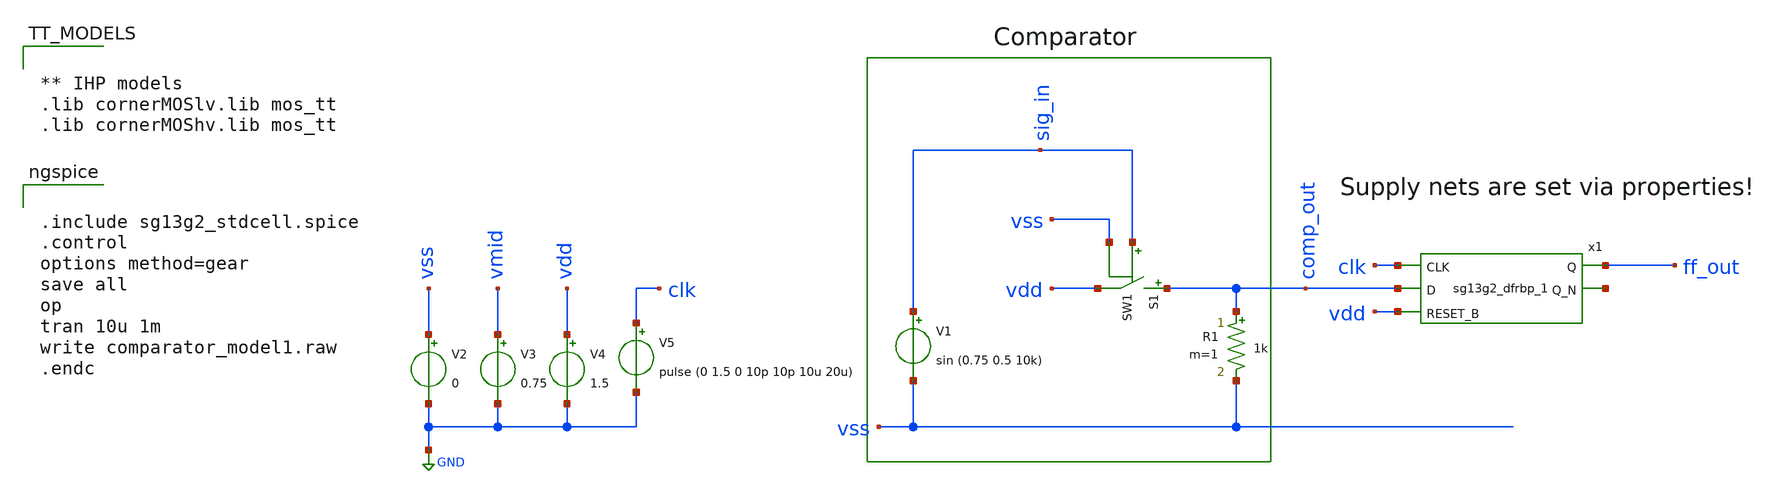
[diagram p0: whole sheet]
** sch_path: 10_xschem/comparator_model1.sch
**.subckt comparator_model1
S1 comp_out vdd sig_in vss SW1
R1 comp_out vss 1k m=1
V1 sig_in vss sin (0.75 0.5 10k)
V2 vss GND 0
V3 vmid GND 0.75
V4 vdd GND 1.5
x1 ff_out net1 clk comp_out vdd vdd vss sg13g2_dfrbp_1
V5 clk GND pulse (0 1.5 0 10p 10p 10u 20u)
**** begin user architecture code


.include sg13g2_stdcell.spice
.control
options method=gear
save all
op
tran 10u 1m
write comparator_model1.raw
.endc




** IHP models
.lib cornerMOSlv.lib mos_tt
.lib cornerMOShv.lib mos_tt


**** end user architecture code
**.ends

* expanding   symbol:  sg13g2_stdcells/sg13g2_dfrbp_1.sym # of pins=5
** sym_path: sg13g2_stdcells/sg13g2_dfrbp_1.sym
** sch_path: sg13g2_stdcells/sg13g2_dfrbp_1.sch
.subckt sg13g2_dfrbp_1 Q Q_N CLK D RESET_B VDD VSS
*.ipin D
*.ipin RESET_B
*.ipin CLK
*.opin Q
*.opin Q_N
*.iopin VDD
*.iopin VSS
XM1 Db D net10 VSS sg13_lv_nmos w=420.00n l=130.00n ng=1 m=1 mm_ok=1
XM2 net10 RESET_B VSS VSS sg13_lv_nmos w=420.00n l=130.00n ng=1 m=1 mm_ok=1
XM3 net1 clkneg net9 VSS sg13_lv_nmos w=420.00n l=130.00n ng=1 m=1 mm_ok=1
XM4 net9 net1 VSS VSS sg13_lv_nmos w=420.00n l=130.00n ng=1 m=1 mm_ok=1
XM5 net1 net1 net5 VSS sg13_lv_nmos w=420.00n l=130.00n ng=1 m=1 mm_ok=1
XM6 net5 RESET_B VSS VSS sg13_lv_nmos w=420.00n l=130.00n ng=1 m=1 mm_ok=1
XM7 Q_N net1 VSS VSS sg13_lv_nmos w=740.00n l=130.00n ng=1 m=1 mm_ok=1
XM8 net2 net1 VSS VSS sg13_lv_nmos w=740.00n l=130.00n ng=1 m=1 mm_ok=1
XM9 Q net2 VSS VSS sg13_lv_nmos w=740.00n l=130.00n ng=1 m=1 mm_ok=1
XM10 clkneg CLK VSS VSS sg13_lv_nmos w=740.00n l=130.00n ng=1 m=1 mm_ok=1
XM11 clkpos clkneg VSS VSS sg13_lv_nmos w=740.00n l=130.00n ng=1 m=1 mm_ok=1
XM12 Db clkneg net3 VSS sg13_lv_nmos w=420.00n l=130.00n ng=1 m=1 mm_ok=1
XM13 net3 clkpos net8 VSS sg13_lv_nmos w=420.00n l=130.00n ng=1 m=1 mm_ok=1
XM14 net8 net3 net4 VSS sg13_lv_nmos w=420.00n l=130.00n ng=1 m=1 mm_ok=1
XM15 net4 RESET_B VSS VSS sg13_lv_nmos w=420.00n l=130.00n ng=1 m=1 mm_ok=1
XM16 net3 net3 VSS VSS sg13_lv_nmos w=740.00n l=130.00n ng=1 m=1 mm_ok=1
XM17 net3 clkpos net1 VSS sg13_lv_nmos w=740.00n l=130.00n ng=1 m=1 mm_ok=1
XM18 Db RESET_B VDD VDD sg13_lv_pmos w=420.00n l=130.00n ng=1 m=1 mm_ok=1
XM19 Db D VDD VDD sg13_lv_pmos w=420.00n l=130.00n ng=1 m=1 mm_ok=1
XM20 net7 net1 VDD VDD sg13_lv_pmos w=420.00n l=130.00n ng=1 m=1 mm_ok=1
XM21 net1 clkpos net7 VDD sg13_lv_pmos w=420.00n l=130.00n ng=1 m=1 mm_ok=1
XM22 net1 net1 VDD VDD sg13_lv_pmos w=420.00n l=130.00n ng=1 m=1 mm_ok=1
XM23 net1 RESET_B VDD VDD sg13_lv_pmos w=420.00n l=130.00n ng=1 m=1 mm_ok=1
XM24 Q_N net1 VDD VDD sg13_lv_pmos w=1.12u l=130.00n ng=1 m=1 mm_ok=1
XM25 net2 net1 VDD VDD sg13_lv_pmos w=1.12u l=130.00n ng=1 m=1 mm_ok=1
XM26 Q net2 VDD VDD sg13_lv_pmos w=1.12u l=130.00n ng=1 m=1 mm_ok=1
XM27 clkneg CLK VDD VDD sg13_lv_pmos w=1.12u l=130.00n ng=1 m=1 mm_ok=1
XM28 clkpos clkneg VDD VDD sg13_lv_pmos w=1.12u l=130.00n ng=1 m=1 mm_ok=1
XM29 Db clkpos net3 VDD sg13_lv_pmos w=420.00n l=130.00n ng=1 m=1 mm_ok=1
XM30 net6 net3 VDD VDD sg13_lv_pmos w=420.00n l=130.00n ng=1 m=1 mm_ok=1
XM31 net3 clkneg net6 VDD sg13_lv_pmos w=420.00n l=130.00n ng=1 m=1 mm_ok=1
XM32 net3 RESET_B VDD VDD sg13_lv_pmos w=420.00n l=130.00n ng=1 m=1 mm_ok=1
XM33 net3 net3 VDD VDD sg13_lv_pmos w=1.000u l=130.00n ng=1 m=1 mm_ok=1
XM34 net3 clkneg net1 VDD sg13_lv_pmos w=1.000u l=130.00n ng=1 m=1 mm_ok=1
.ends

.GLOBAL GND
**** begin user architecture code
.MODEL SW1 SW( VT=0.75 VH=0 RON=0.01 ROFF=10G )
**** end user architecture code
.end
